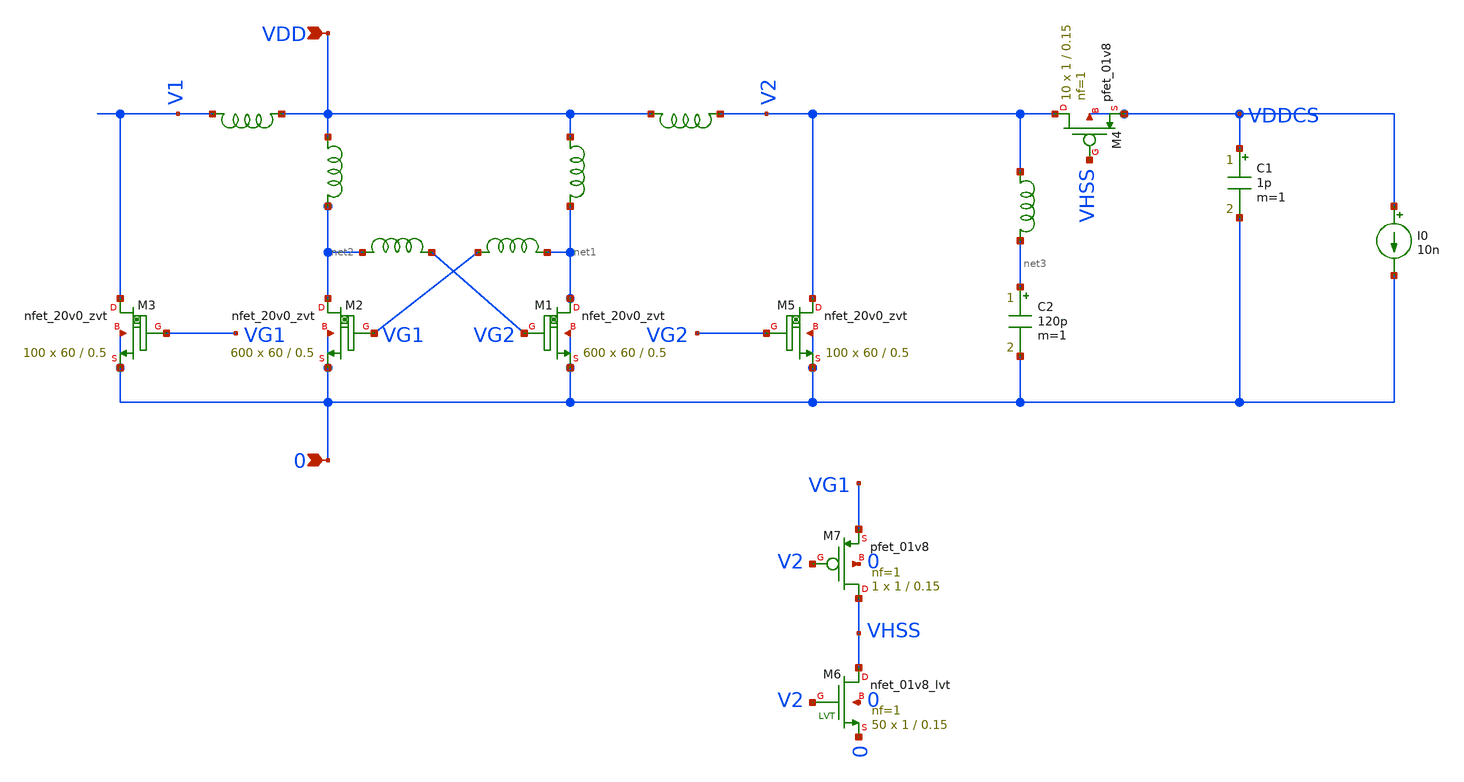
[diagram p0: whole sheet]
** sch_path: design/LELO_SVOD_SKY130A/LELO_EXSC.sch
**.subckt LELO_EXSC 0 VDD
*.ipin 0
*.ipin VDD
x3 VDD net1 1812PS-102_imp
x4 VDD net2 1812PS-102_imp
XM1 net1 VG2 0 0 sky130_fd_pr__nfet_20v0_zvt W=60 L=0.5 m=600
XM2 net2 VG1 0 0 sky130_fd_pr__nfet_20v0_zvt W=60 L=0.5 m=600
x1 net2 VG2 1812PS-104_imp
x2 VG1 net1 1812PS-104_imp
C1 VDDCS 0 1p m=1
XM3 V1 VG1 0 0 sky130_fd_pr__nfet_20v0_zvt W=60 L=0.5 m=100
XM5 V2 VG2 0 0 sky130_fd_pr__nfet_20v0_zvt W=60 L=0.5 m=100
C2 net3 0 120p m=1
x5 VDD V1 1812PS-223_imp
XM6 VHSS V2 0 0 sky130_fd_pr__nfet_01v8_lvt L=0.15 W=1 nf=1 ad='int((1 + 1)/2) * 1 / 1 * 0.29' as='int((1 + 2)/2) * 1 / 1 * 0.29'
+ pd='2*int((1 + 1)/2) * (1 / 1 + 0.29)' ps='2*int((1 + 2)/2) * (1 / 1 + 0.29)' nrd='0.29 / 1 ' nrs='0.29 / 1 '
+ sa=0 sb=0 sd=0 mult=50 m=50
XM4 V2 VHSS VDDCS VDDCS sky130_fd_pr__pfet_01v8 L=0.15 W=1 nf=1 ad='int((1 + 1)/2) * 1 / 1 * 0.29' as='int((1 + 2)/2) * 1 / 1 * 0.29'
+ pd='2*int((1 + 1)/2) * (1 / 1 + 0.29)' ps='2*int((1 + 2)/2) * (1 / 1 + 0.29)' nrd='0.29 / 1 ' nrs='0.29 / 1 '
+ sa=0 sb=0 sd=0 mult=10 m=10
XM7 VHSS V2 VG1 0 sky130_fd_pr__pfet_01v8 L=0.15 W=1 nf=1 ad='int((1 + 1)/2) * 1 / 1 * 0.29' as='int((1 + 2)/2) * 1 / 1 * 0.29'
+ pd='2*int((1 + 1)/2) * (1 / 1 + 0.29)' ps='2*int((1 + 2)/2) * (1 / 1 + 0.29)' nrd='0.29 / 1 ' nrs='0.29 / 1 '
+ sa=0 sb=0 sd=0 mult=1 m=1
I0 VDDCS 0 10n
x7 V2 net3 1812PS-334_imp
x6 V2 VDD 1812PS-334_imp
**.ends

* expanding   symbol:  LELO_SVOD_SKY130A/1812PS-102_imp.sym # of pins=2
** sym_path: design/LELO_SVOD_SKY130A/1812PS-102_imp.sym

.subckt 1812PS-102_imp port1 port2
X1 port1 port2 Model1D R1=60 R2=0.054 C= 0.15p K1=0.000001 K2=0.064 K3= 1u K4=1E-06 K5=0.000001 L=0
+ Is=0 a=0 L_Z0=0 L_EL=0 L_F0=0E6 PkZ=1282.46492
.ends 1812PS-102_imp

* expanding   symbol:  LELO_SVOD_SKY130A/1812PS-104_imp.sym # of pins=2
** sym_path: design/LELO_SVOD_SKY130A/1812PS-104_imp.sym

.subckt 1812PS-104_imp port1 port2
X1 port1 port2 Model1D R1=40 R2=1.3 C= 1.6p K1=0.000001 K2=13.98 K3= 100u K4=0.000001 K5=0.000001
+ L=0 Is=0 a=0 L_Z0=0 L_EL=0 L_F0=0E6 PkZ=48065.0165
.ends 1812PS-104_imp

* expanding   symbol:  LELO_SVOD_SKY130A/1812PS-223_imp.sym # of pins=2
** sym_path: design/LELO_SVOD_SKY130A/1812PS-223_imp.sym

.subckt 1812PS-223_imp port1 port2
X1 port1 port2 Model1D R1=45 R2=0.33 C= 0.6p K1=0.000001 K2=2.28 K3= 22u K4=0.000001 K5=0.0000351
+ L=0 Is=0 a=0 L_Z0=0 L_EL=0 L_F0=0E6 PkZ=14816.336
.ends 1812PS-223_imp

* expanding   symbol:  LELO_SVOD_SKY130A/1812PS-334_imp.sym # of pins=2
** sym_path: design/LELO_SVOD_SKY130A/1812PS-334_imp.sym

.subckt 1812PS-334_imp port1 port2
X1 port1 port2 Model1D R1=75 R2=4.9 C= 2.43p K1=1E-06 K2=57.9 K3= 330u K4=0.000001 K5=0.000001 L=0
+ Is=0 a=0 L_Z0=0 L_EL=0 L_F0=0E6 PkZ=127597.141
.ends 1812PS-334_imp

.end
